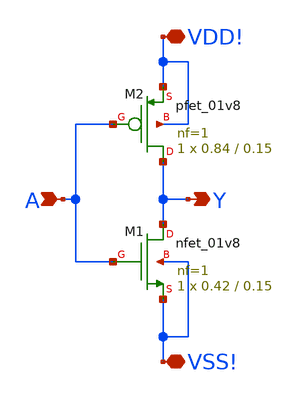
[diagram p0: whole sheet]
** sch_path: inv1X/inv1X.sch
**.subckt inv1X A Y VDD! VSS!
*.ipin A
*.opin Y
*.iopin VDD!
*.iopin VSS!
XM1 Y A VSS! VSS! sky130_fd_pr__nfet_01v8 L=0.15 W=0.42 nf=1 ad='int((1 + 1)/2) * 0.42 / 1 * 0.29' as='int((1 + 2)/2) * 0.42 / 1 * 0.29'
+ pd='2*int((1 + 1)/2) * (0.42 / 1 + 0.29)' ps='2*int((1 + 2)/2) * (0.42 / 1 + 0.29)' nrd='0.29 / 0.42 '
+ nrs='0.29 / 0.42 ' sa=0 sb=0 sd=0 mult=1 m=1
XM2 Y A VDD! VDD! sky130_fd_pr__pfet_01v8 L=0.15 W=0.84 nf=1 ad='int((1 + 1)/2) * 0.84 / 1 * 0.29' as='int((1 + 2)/2) * 0.84 / 1 * 0.29'
+ pd='2*int((1 + 1)/2) * (0.84 / 1 + 0.29)' ps='2*int((1 + 2)/2) * (0.84 / 1 + 0.29)' nrd='0.29 / 0.84 '
+ nrs='0.29 / 0.84 ' sa=0 sb=0 sd=0 mult=1 m=1
**.ends
.end
